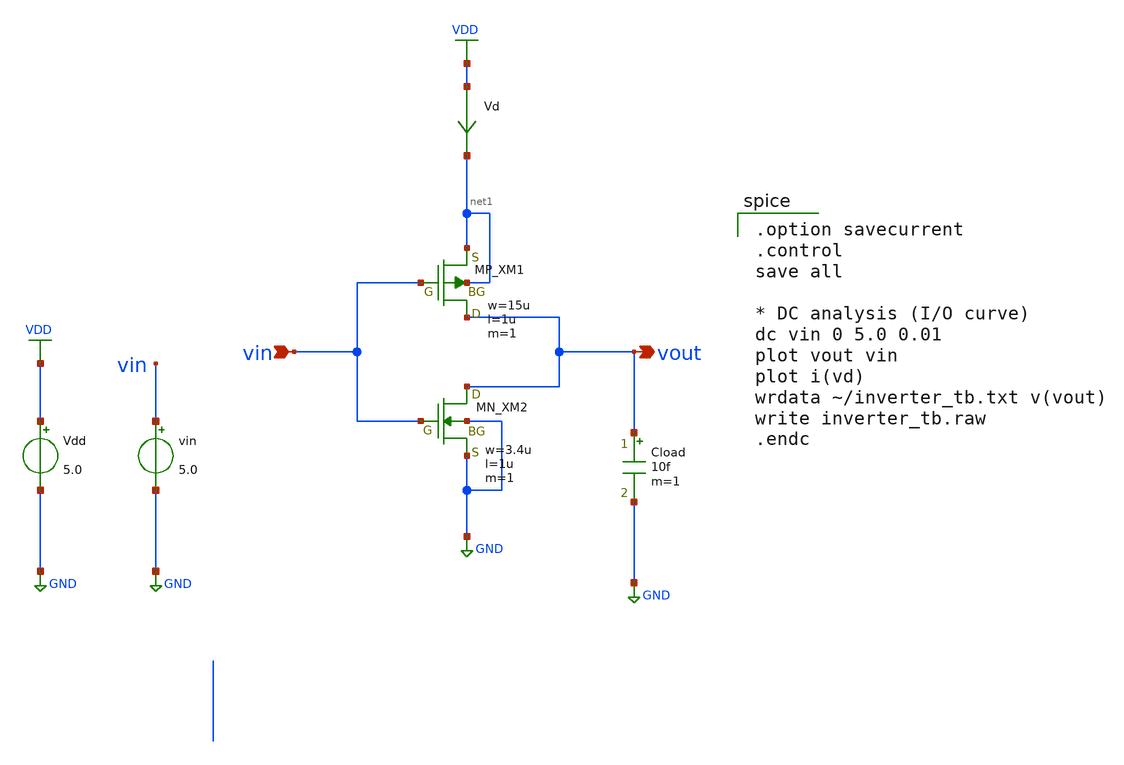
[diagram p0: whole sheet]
** sch_path: inverter/inverter_Tsukasa_Yamamoto_tb.sch
**.subckt inverter_Tsukasa_Yamamoto_tb vin vout
*.ipin vin
*.opin vout
XXM1 vout vin net1 net1 PMOS w=15u l=1u nrd=0 nrs=0 m=1
XXM2 vout vin GND GND NMOS w=3.4u l=1u nrd=0 nrs=0 m=1
Vdd VDD GND 5.0
vin vin GND 5.0
Cload vout GND 10f m=1
Vd VDD net1 0
.save i(vd)
**** begin user architecture code
 .include $::LIB/ip62_models

.option savecurrent
.control
save all

* DC analysis (I/O curve)
dc vin 0 5.0 0.01
plot vout vin
plot i(vd)
wrdata ~/inverter_tb.txt v(vout)
write inverter_tb.raw
.endc

**** end user architecture code
**.ends
.GLOBAL GND
.GLOBAL VDD
.end
